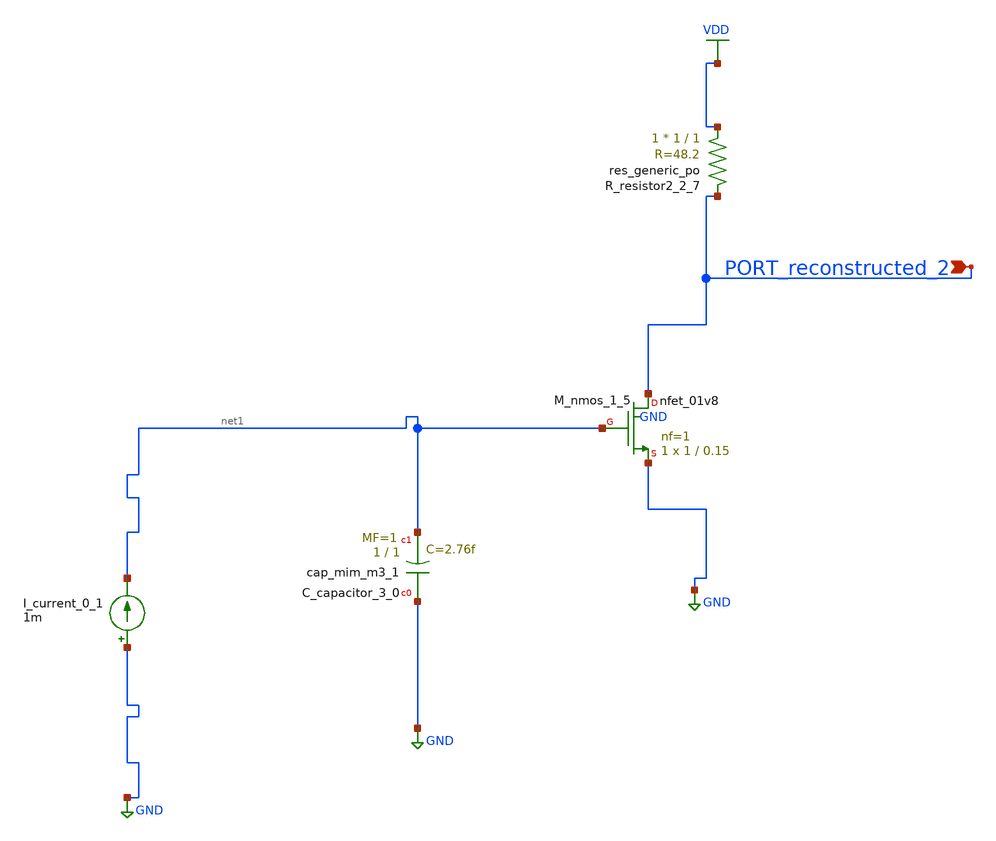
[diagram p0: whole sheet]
** sch_path: schematics/AMSNet/503.sch
**.subckt 503 PORT_reconstructed_2
*.ipin PORT_reconstructed_2
XC_capacitor_3_0 GND net1 sky130_fd_pr__cap_mim_m3_1 W=1 L=1 MF=1 m=1
I_current_0_1 GND net1 1m
XM_nmos_1_5 PORT_reconstructed_2 net1 GND GND sky130_fd_pr__nfet_01v8 L=0.15 W=1 nf=1 ad='int((1 + 1)/2) * 1 / 1 * 0.29'
+ as='int((1 + 2)/2) * 1 / 1 * 0.29' pd='2*int((1 + 1)/2) * (1 / 1 + 0.29)' ps='2*int((1 + 2)/2) * (1 / 1 + 0.29)'
+ nrd='0.29 / 1 ' nrs='0.29 / 1 ' sa=0 sb=0 sd=0 mult=1 m=1
XR_resistor2_2_7 VDD PORT_reconstructed_2 sky130_fd_pr__res_generic_po W=1 L=1 m=1
**.ends
.GLOBAL GND
.GLOBAL VDD
.end
